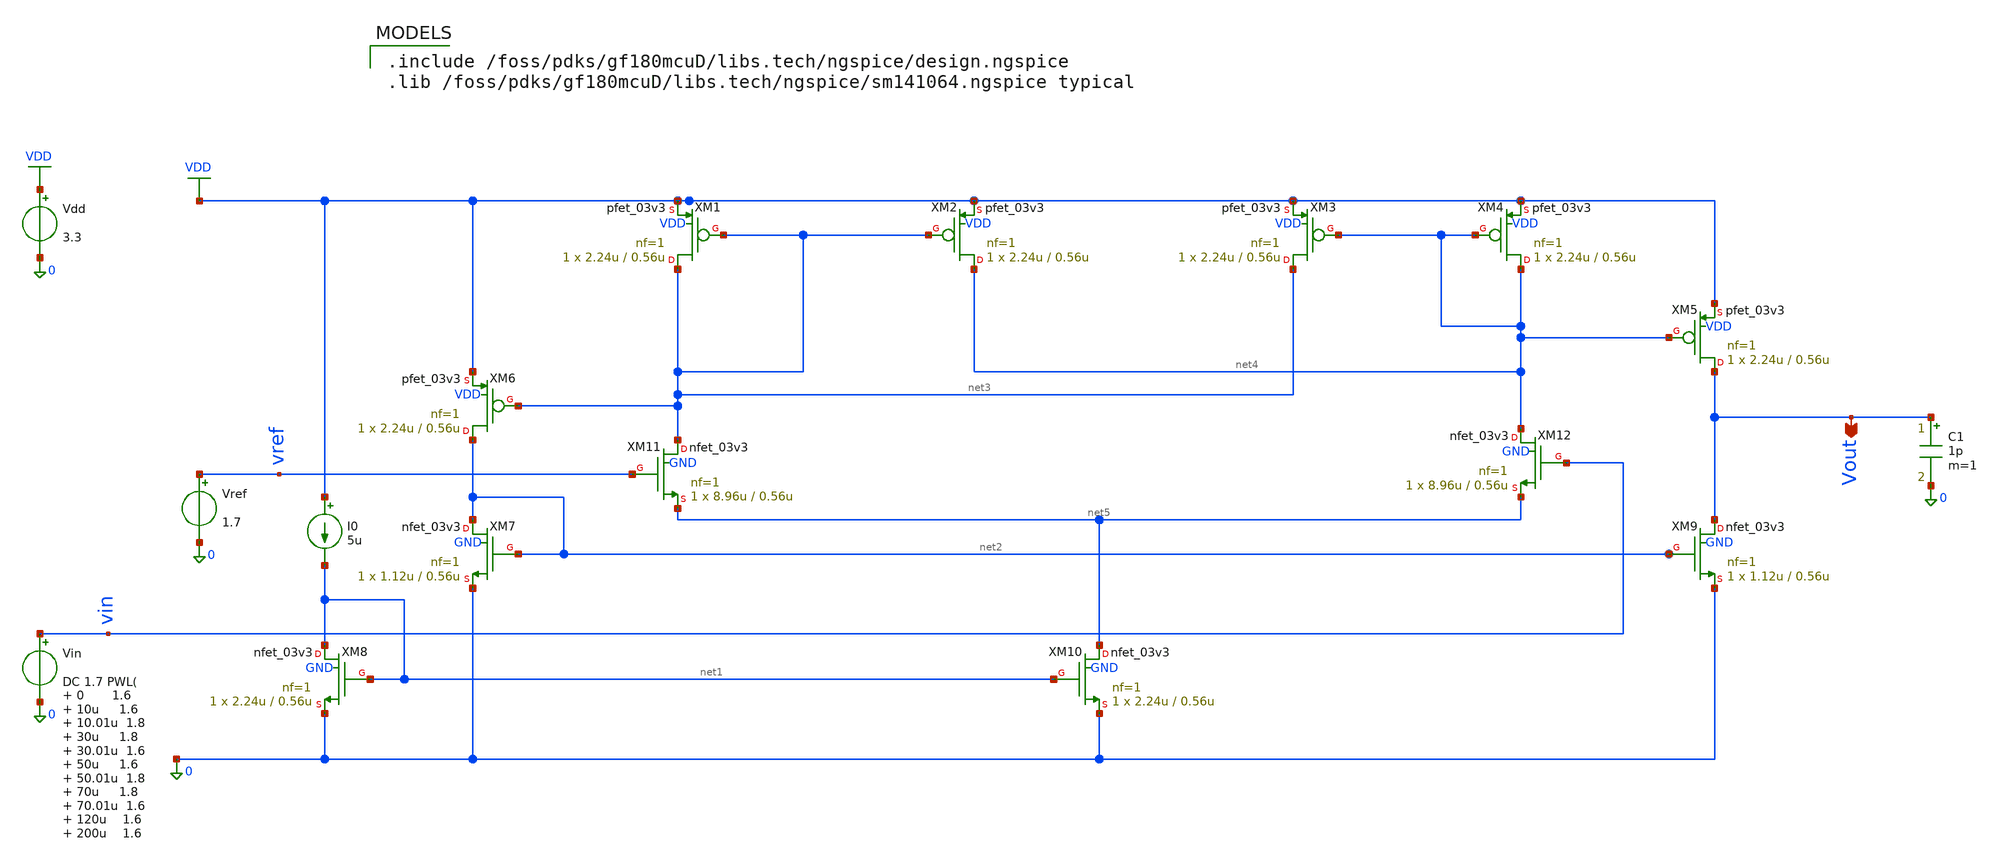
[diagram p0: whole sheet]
** sch_path: comparator/schematic-design/comparator_sim.sch
**.subckt comparator_sim Vout
*.opin Vout
XM1 net3 net3 VDD VDD pfet_03v3 L=0.56u W=2.24u nf=1 ad='int((nf+1)/2) * W/nf * 0.18u' as='int((nf+2)/2) * W/nf * 0.18u'
+ pd='2*int((nf+1)/2) * (W/nf + 0.18u)' ps='2*int((nf+2)/2) * (W/nf + 0.18u)' nrd='0.18u / W' nrs='0.18u / W'
+ sa=0 sb=0 sd=0 m=1 par=1
XM2 net4 net3 VDD VDD pfet_03v3 L=0.56u W=2.24u nf=1 ad='int((nf+1)/2) * W/nf * 0.18u' as='int((nf+2)/2) * W/nf * 0.18u'
+ pd='2*int((nf+1)/2) * (W/nf + 0.18u)' ps='2*int((nf+2)/2) * (W/nf + 0.18u)' nrd='0.18u / W' nrs='0.18u / W'
+ sa=0 sb=0 sd=0 m=1 par=1
XM3 net3 net4 VDD VDD pfet_03v3 L=0.56u W=2.24u nf=1 ad='int((nf+1)/2) * W/nf * 0.18u' as='int((nf+2)/2) * W/nf * 0.18u'
+ pd='2*int((nf+1)/2) * (W/nf + 0.18u)' ps='2*int((nf+2)/2) * (W/nf + 0.18u)' nrd='0.18u / W' nrs='0.18u / W'
+ sa=0 sb=0 sd=0 m=1 par=1
XM4 net4 net4 VDD VDD pfet_03v3 L=0.56u W=2.24u nf=1 ad='int((nf+1)/2) * W/nf * 0.18u' as='int((nf+2)/2) * W/nf * 0.18u'
+ pd='2*int((nf+1)/2) * (W/nf + 0.18u)' ps='2*int((nf+2)/2) * (W/nf + 0.18u)' nrd='0.18u / W' nrs='0.18u / W'
+ sa=0 sb=0 sd=0 m=1 par=1
XM5 Vout net4 VDD VDD pfet_03v3 L=0.56u W=2.24u nf=1 ad='int((nf+1)/2) * W/nf * 0.18u' as='int((nf+2)/2) * W/nf * 0.18u'
+ pd='2*int((nf+1)/2) * (W/nf + 0.18u)' ps='2*int((nf+2)/2) * (W/nf + 0.18u)' nrd='0.18u / W' nrs='0.18u / W'
+ sa=0 sb=0 sd=0 m=1 par=1
XM6 net2 net3 VDD VDD pfet_03v3 L=0.56u W=2.24u nf=1 ad='int((nf+1)/2) * W/nf * 0.18u' as='int((nf+2)/2) * W/nf * 0.18u'
+ pd='2*int((nf+1)/2) * (W/nf + 0.18u)' ps='2*int((nf+2)/2) * (W/nf + 0.18u)' nrd='0.18u / W' nrs='0.18u / W'
+ sa=0 sb=0 sd=0 m=1 par=1
XM7 net2 net2 0 GND nfet_03v3 L=0.56u W=1.12u nf=1 ad='int((nf+1)/2) * W/nf * 0.18u' as='int((nf+2)/2) * W/nf * 0.18u'
+ pd='2*int((nf+1)/2) * (W/nf + 0.18u)' ps='2*int((nf+2)/2) * (W/nf + 0.18u)' nrd='0.18u / W' nrs='0.18u / W'
+ sa=0 sb=0 sd=0 m=1 par=1
XM8 net1 net1 0 GND nfet_03v3 L=0.56u W=2.24u nf=1 ad='int((nf+1)/2) * W/nf * 0.18u' as='int((nf+2)/2) * W/nf * 0.18u'
+ pd='2*int((nf+1)/2) * (W/nf + 0.18u)' ps='2*int((nf+2)/2) * (W/nf + 0.18u)' nrd='0.18u / W' nrs='0.18u / W'
+ sa=0 sb=0 sd=0 m=1 par=1
XM9 Vout net2 0 GND nfet_03v3 L=0.56u W=1.12u nf=1 ad='int((nf+1)/2) * W/nf * 0.18u' as='int((nf+2)/2) * W/nf * 0.18u'
+ pd='2*int((nf+1)/2) * (W/nf + 0.18u)' ps='2*int((nf+2)/2) * (W/nf + 0.18u)' nrd='0.18u / W' nrs='0.18u / W'
+ sa=0 sb=0 sd=0 m=1 par=1
XM10 net5 net1 0 GND nfet_03v3 L=0.56u W=2.24u nf=1 ad='int((nf+1)/2) * W/nf * 0.18u' as='int((nf+2)/2) * W/nf * 0.18u'
+ pd='2*int((nf+1)/2) * (W/nf + 0.18u)' ps='2*int((nf+2)/2) * (W/nf + 0.18u)' nrd='0.18u / W' nrs='0.18u / W'
+ sa=0 sb=0 sd=0 m=1 par=1
XM11 net3 vref net5 GND nfet_03v3 L=0.56u W=8.96u nf=1 ad='int((nf+1)/2) * W/nf * 0.18u' as='int((nf+2)/2) * W/nf * 0.18u'
+ pd='2*int((nf+1)/2) * (W/nf + 0.18u)' ps='2*int((nf+2)/2) * (W/nf + 0.18u)' nrd='0.18u / W' nrs='0.18u / W'
+ sa=0 sb=0 sd=0 m=1 par=1
XM12 net4 vin net5 GND nfet_03v3 L=0.56u W=8.96u nf=1 ad='int((nf+1)/2) * W/nf * 0.18u' as='int((nf+2)/2) * W/nf * 0.18u'
+ pd='2*int((nf+1)/2) * (W/nf + 0.18u)' ps='2*int((nf+2)/2) * (W/nf + 0.18u)' nrd='0.18u / W' nrs='0.18u / W'
+ sa=0 sb=0 sd=0 m=1 par=1
I0 VDD net1 5u
Vref vref 0 1.7
Vin vin 0 DC 1.7 PWL( 0 1.6 10u 1.6 10.01u 1.8 30u 1.8 30.01u 1.6 50u 1.6 50.01u 1.8 70u 1.8 70.01u
+ 1.6 120u 1.6 200u 1.6 300u 1.8 400u 1.6 420u 1.6
)

Vdd VDD 0 3.3
C1 Vout 0 1p m=1
**** begin user architecture code

.include /foss/pdks/gf180mcuD/libs.tech/ngspice/design.ngspice
.lib /foss/pdks/gf180mcuD/libs.tech/ngspice/sm141064.ngspice typical


.control
set noaskquit
save all

* ============================================================
* 0. OPERATING POINT FOR GM/ID ANNOTATION
* ============================================================

op
write comparator_op.raw all

* ============================================================
* 1. DC TRANSFER AND NOMINAL OFFSET
* ============================================================

dc Vin 1.60 1.80 0.1m

meas dc vtrip_nom find v(vin) when v(vout)=1.65 rise=1
let vos_nom_mV = (vtrip_nom - 1.7) * 1e3

echo
echo ------------------------------------------------------------
echo NOMINAL DC OFFSET
echo Target magnitude: less than 1 mV to 5 mV
echo Actual in mV:
print vos_nom_mV

if (abs(vos_nom_mV) <= 5)
  echo Status: PASS
else
  echo Status: FAIL
end

write comparator_dc.raw all


* ============================================================
* 2. TRANSIENT ANALYSIS
* ============================================================

tran 10n 420u

write comparator_all_tran.raw all


* ============================================================
* 3. INPUT AND OUTPUT SWING
* ============================================================

meas tran vin_high  max v(vin)  from=5u to=120u
meas tran vin_low   min v(vin)  from=5u to=120u
meas tran vout_high max v(vout) from=5u to=120u
meas tran vout_low  min v(vout) from=5u to=120u


* ============================================================
* 4. PROPAGATION DELAY — NONINVERTING OUTPUT
* ============================================================

meas tran tpd_rise trig v(vin) val=1.7 rise=1 td=5u  targ v(vout) val=1.65 rise=1 td=5u

meas tran tpd_fall trig v(vin) val=1.7 fall=1 td=20u  targ v(vout) val=1.65 fall=1 td=20u


* ============================================================
* 5. AVERAGE CURRENT AND POWER
* ============================================================

meas tran idd_avg avg i(Vdd) from=10u to=120u

let pavg = abs(3.3 * idd_avg)


* ============================================================
* 6. HYSTERESIS
* ============================================================

meas tran vtrip_up find v(vin)  when v(vout)=1.65 rise=1 td=200u

meas tran vtrip_down find v(vin)  when v(vout)=1.65 fall=1 td=300u

let vhyst = abs(vtrip_up - vtrip_down)
let vhyst_center = (vtrip_up + vtrip_down) / 2


* ============================================================
* 7. CONVERT RESULTS TO DISPLAY UNITS
* ============================================================

let vhyst_mV       = vhyst * 1e3
let tpd_rise_us    = tpd_rise * 1e6
let tpd_fall_us    = tpd_fall * 1e6
let pavg_uW        = pavg * 1e6
let idd_avg_uA     = abs(idd_avg) * 1e6
let center_error_mV = abs(vhyst_center - 1.7) * 1e3


* ============================================================
* 8. PRINT SPECIFICATION SUMMARY
* ============================================================

echo
echo ============================================================
echo              COMPARATOR SIMULATION SUMMARY
echo ============================================================
echo
echo HYSTERESIS
echo Target: 2 mV to 5 mV
echo Actual:
print vhyst_mV

if (vhyst_mV >= 2)
  if (vhyst_mV <= 5)
    echo Status: PASS
  else
    echo Status: FAIL
  end
else
  echo Status: FAIL
end

echo
echo ------------------------------------------------------------
echo RISE PROPAGATION DELAY
echo Target: less than 10 us
echo Actual:
print tpd_rise_us

if (tpd_rise_us < 10)
  echo Status: PASS
else
  echo Status: FAIL
end

echo
echo ------------------------------------------------------------
echo FALL PROPAGATION DELAY
echo Target: less than 10 us
echo Actual:
print tpd_fall_us

if (tpd_fall_us < 10)
  echo Status: PASS
else
  echo Status: FAIL
end

echo
echo ------------------------------------------------------------
echo AVERAGE SUPPLY CURRENT
echo Actual in uA:
print idd_avg_uA

echo
echo ------------------------------------------------------------
echo AVERAGE POWER
echo Preferred target: less than 100 uW
echo Maximum target: less than 200 uW
echo Actual:
print pavg_uW

if (pavg_uW < 100)
  echo Status: PASS - below preferred limit
else
  if (pavg_uW < 200)
    echo Status: PASS - below maximum limit
  else
    echo Status: FAIL
  end
end

echo
echo ------------------------------------------------------------
echo OUTPUT SWING
echo Target: approximately 0 V to 3.3 V
echo Actual high:
print vout_high
echo Actual low:
print vout_low

if (vout_high > 3.2)
  if (vout_low < 0.1)
    echo Status: PASS
  else
    echo Status: FAIL
  end
else
  echo Status: FAIL
end

echo
echo ------------------------------------------------------------
echo HYSTERESIS CENTER
echo Target: Vref = 1.7 V
echo Actual center:
print vhyst_center
echo Center error in mV:
print center_error_mV

if (center_error_mV < 5)
  echo Status: PASS
else
  echo Status: FAIL
end

echo
echo ------------------------------------------------------------
echo TRIP POINTS
echo Vtrip up:
print vtrip_up
echo Vtrip down:
print vtrip_down

echo
echo ============================================================
echo                  END OF SUMMARY
echo ============================================================
echo

.endc

**** end user architecture code
**.ends
.GLOBAL VDD
.end
